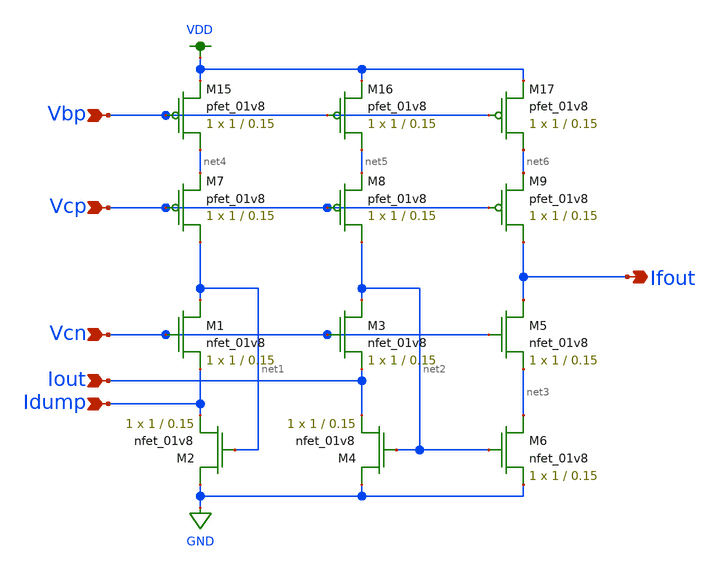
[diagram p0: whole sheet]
** sch_path: FVF-1.sch
**.subckt FVF-1 Vcn Iout Idump Vcp Vbp Ifout
*.ipin Vcn
*.ipin Iout
*.ipin Idump
*.ipin Vcp
*.ipin Vbp
*.opin Ifout
XM1 net1 Vcn Idump GND sky130_fd_pr__nfet_01v8 L=0.15 W=1 nf=1 ad='int((nf+1)/2) * W/nf * 0.29' as='int((nf+2)/2) * W/nf * 0.29'
+ pd='2*int((nf+1)/2) * (W/nf + 0.29)' ps='2*int((nf+2)/2) * (W/nf + 0.29)' nrd='0.29 / W' nrs='0.29 / W'
+ sa=0 sb=0 sd=0 mult=1 m=1
XM2 GND net1 Idump GND sky130_fd_pr__nfet_01v8 L=0.15 W=1 nf=1 ad='int((nf+1)/2) * W/nf * 0.29' as='int((nf+2)/2) * W/nf * 0.29'
+ pd='2*int((nf+1)/2) * (W/nf + 0.29)' ps='2*int((nf+2)/2) * (W/nf + 0.29)' nrd='0.29 / W' nrs='0.29 / W'
+ sa=0 sb=0 sd=0 mult=1 m=1
XM3 net2 Vcn Iout GND sky130_fd_pr__nfet_01v8 L=0.15 W=1 nf=1 ad='int((nf+1)/2) * W/nf * 0.29' as='int((nf+2)/2) * W/nf * 0.29'
+ pd='2*int((nf+1)/2) * (W/nf + 0.29)' ps='2*int((nf+2)/2) * (W/nf + 0.29)' nrd='0.29 / W' nrs='0.29 / W'
+ sa=0 sb=0 sd=0 mult=1 m=1
XM4 GND net2 Iout GND sky130_fd_pr__nfet_01v8 L=0.15 W=1 nf=1 ad='int((nf+1)/2) * W/nf * 0.29' as='int((nf+2)/2) * W/nf * 0.29'
+ pd='2*int((nf+1)/2) * (W/nf + 0.29)' ps='2*int((nf+2)/2) * (W/nf + 0.29)' nrd='0.29 / W' nrs='0.29 / W'
+ sa=0 sb=0 sd=0 mult=1 m=1
XM5 Ifout Vcn net3 GND sky130_fd_pr__nfet_01v8 L=0.15 W=1 nf=1 ad='int((nf+1)/2) * W/nf * 0.29' as='int((nf+2)/2) * W/nf * 0.29'
+ pd='2*int((nf+1)/2) * (W/nf + 0.29)' ps='2*int((nf+2)/2) * (W/nf + 0.29)' nrd='0.29 / W' nrs='0.29 / W'
+ sa=0 sb=0 sd=0 mult=1 m=1
XM6 net3 net2 GND GND sky130_fd_pr__nfet_01v8 L=0.15 W=1 nf=1 ad='int((nf+1)/2) * W/nf * 0.29' as='int((nf+2)/2) * W/nf * 0.29'
+ pd='2*int((nf+1)/2) * (W/nf + 0.29)' ps='2*int((nf+2)/2) * (W/nf + 0.29)' nrd='0.29 / W' nrs='0.29 / W'
+ sa=0 sb=0 sd=0 mult=1 m=1
XM7 net1 Vcp net4 VDD sky130_fd_pr__pfet_01v8 L=0.15 W=1 nf=1 ad='int((nf+1)/2) * W/nf * 0.29' as='int((nf+2)/2) * W/nf * 0.29'
+ pd='2*int((nf+1)/2) * (W/nf + 0.29)' ps='2*int((nf+2)/2) * (W/nf + 0.29)' nrd='0.29 / W' nrs='0.29 / W'
+ sa=0 sb=0 sd=0 mult=1 m=1
XM8 net2 Vcp net5 VDD sky130_fd_pr__pfet_01v8 L=0.15 W=1 nf=1 ad='int((nf+1)/2) * W/nf * 0.29' as='int((nf+2)/2) * W/nf * 0.29'
+ pd='2*int((nf+1)/2) * (W/nf + 0.29)' ps='2*int((nf+2)/2) * (W/nf + 0.29)' nrd='0.29 / W' nrs='0.29 / W'
+ sa=0 sb=0 sd=0 mult=1 m=1
XM9 Ifout Vcp net6 VDD sky130_fd_pr__pfet_01v8 L=0.15 W=1 nf=1 ad='int((nf+1)/2) * W/nf * 0.29' as='int((nf+2)/2) * W/nf * 0.29'
+ pd='2*int((nf+1)/2) * (W/nf + 0.29)' ps='2*int((nf+2)/2) * (W/nf + 0.29)' nrd='0.29 / W' nrs='0.29 / W'
+ sa=0 sb=0 sd=0 mult=1 m=1
XM15 net4 Vbp VDD VDD sky130_fd_pr__pfet_01v8 L=0.15 W=1 nf=1 ad='int((nf+1)/2) * W/nf * 0.29' as='int((nf+2)/2) * W/nf * 0.29'
+ pd='2*int((nf+1)/2) * (W/nf + 0.29)' ps='2*int((nf+2)/2) * (W/nf + 0.29)' nrd='0.29 / W' nrs='0.29 / W'
+ sa=0 sb=0 sd=0 mult=1 m=1
XM16 net5 Vbp VDD VDD sky130_fd_pr__pfet_01v8 L=0.15 W=1 nf=1 ad='int((nf+1)/2) * W/nf * 0.29' as='int((nf+2)/2) * W/nf * 0.29'
+ pd='2*int((nf+1)/2) * (W/nf + 0.29)' ps='2*int((nf+2)/2) * (W/nf + 0.29)' nrd='0.29 / W' nrs='0.29 / W'
+ sa=0 sb=0 sd=0 mult=1 m=1
XM17 net6 Vbp VDD VDD sky130_fd_pr__pfet_01v8 L=0.15 W=1 nf=1 ad='int((nf+1)/2) * W/nf * 0.29' as='int((nf+2)/2) * W/nf * 0.29'
+ pd='2*int((nf+1)/2) * (W/nf + 0.29)' ps='2*int((nf+2)/2) * (W/nf + 0.29)' nrd='0.29 / W' nrs='0.29 / W'
+ sa=0 sb=0 sd=0 mult=1 m=1
**.ends
.GLOBAL VDD
.GLOBAL GND
.end
